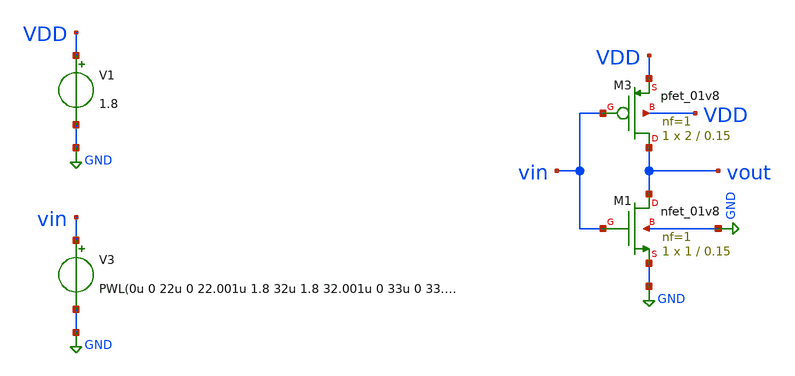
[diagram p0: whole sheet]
** sch_path: schem/inv.sch
**.subckt inv
XM1 vout vin GND GND sky130_fd_pr__nfet_01v8 L=0.15 W=1 nf=1 ad='int((1 + 1)/2) * 1 / 1 * 0.29' as='int((1 + 2)/2) * 1 / 1 * 0.29'
+ pd='2*int((1 + 1)/2) * (1 / 1 + 0.29)' ps='2*int((1 + 2)/2) * (1 / 1 + 0.29)' nrd='0.29 / 1 ' nrs='0.29 / 1 '
+ sa=0 sb=0 sd=0 mult=1 m=1
XM3 vout vin VDD VDD sky130_fd_pr__pfet_01v8 L=0.15 W=2 nf=1 ad='int((1 + 1)/2) * 2 / 1 * 0.29' as='int((1 + 2)/2) * 2 / 1 * 0.29'
+ pd='2*int((1 + 1)/2) * (2 / 1 + 0.29)' ps='2*int((1 + 2)/2) * (2 / 1 + 0.29)' nrd='0.29 / 2 ' nrs='0.29 / 2 '
+ sa=0 sb=0 sd=0 mult=1 m=1
V1 VDD GND 1.8
V3 vin GND PWL(0u 0 22u 0 22.001u 1.8 32u 1.8 32.001u 0 33u 0 33.001u 1.8 43u 1.8 43.001u 0 44u 0)
**** begin user architecture code


.lib /usr/local/share/pdk/sky130A/libs.tech/ngspice/sky130.lib.spice tt

.tran 10n 45u
.save all

.control
    run
    plot vin vout
.endc

.end


**** end user architecture code
**.ends
.GLOBAL GND
.end
